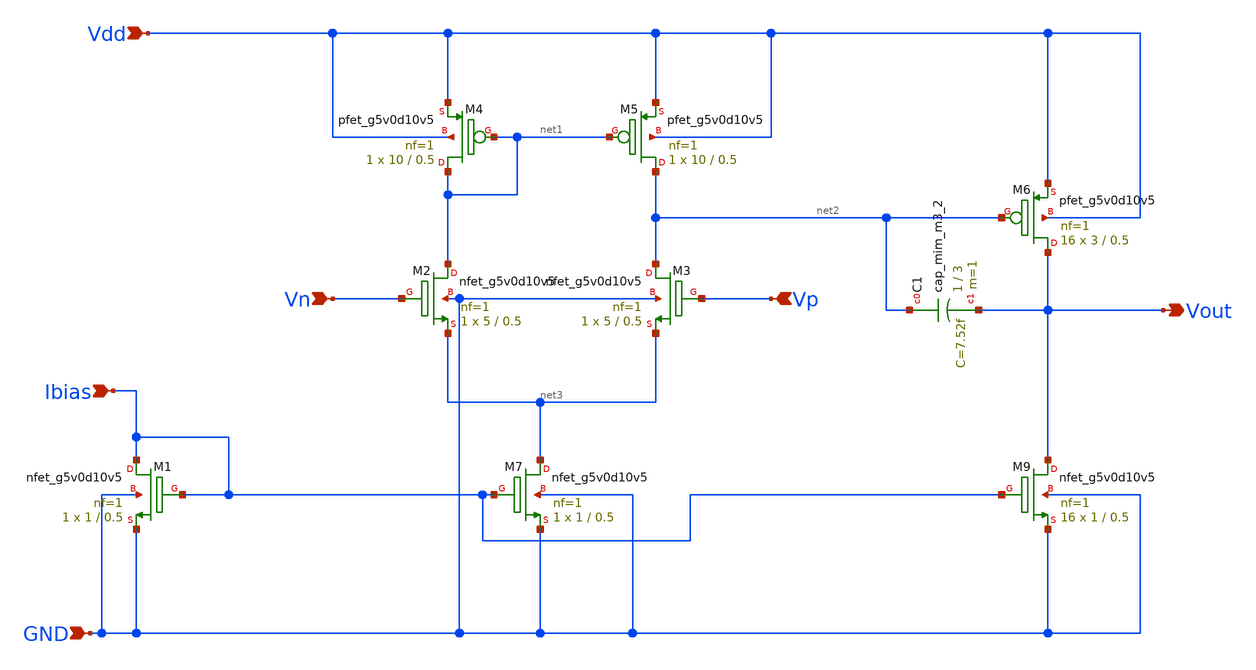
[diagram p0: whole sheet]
** sch_path: Analog_Blocks/LDO/Schematic/LDO_Miller_1.8v/Error_Amplifier.sch
**.subckt Error_Amplifier Vout Vdd GND Vp Vn Ibias
*.opin Vout
*.ipin Vdd
*.ipin GND
*.ipin Vp
*.ipin Vn
*.ipin Ibias
XM2 net1 Vn net3 GND sky130_fd_pr__nfet_g5v0d10v5 L=0.5 W=5 nf=1 ad='int((nf+1)/2) * W/nf * 0.29' as='int((nf+2)/2) * W/nf * 0.29'
+ pd='2*int((nf+1)/2) * (W/nf + 0.29)' ps='2*int((nf+2)/2) * (W/nf + 0.29)' nrd='0.29 / W' nrs='0.29 / W'
+ sa=0 sb=0 sd=0 mult=1 m=1
XM3 net2 Vp net3 GND sky130_fd_pr__nfet_g5v0d10v5 L=0.5 W=5 nf=1 ad='int((nf+1)/2) * W/nf * 0.29' as='int((nf+2)/2) * W/nf * 0.29'
+ pd='2*int((nf+1)/2) * (W/nf + 0.29)' ps='2*int((nf+2)/2) * (W/nf + 0.29)' nrd='0.29 / W' nrs='0.29 / W'
+ sa=0 sb=0 sd=0 mult=1 m=1
XM4 net1 net1 Vdd Vdd sky130_fd_pr__pfet_g5v0d10v5 L=0.5 W=10 nf=1 ad='int((nf+1)/2) * W/nf * 0.29' as='int((nf+2)/2) * W/nf * 0.29'
+ pd='2*int((nf+1)/2) * (W/nf + 0.29)' ps='2*int((nf+2)/2) * (W/nf + 0.29)' nrd='0.29 / W' nrs='0.29 / W'
+ sa=0 sb=0 sd=0 mult=1 m=1
XM5 net2 net1 Vdd Vdd sky130_fd_pr__pfet_g5v0d10v5 L=0.5 W=10 nf=1 ad='int((nf+1)/2) * W/nf * 0.29' as='int((nf+2)/2) * W/nf * 0.29'
+ pd='2*int((nf+1)/2) * (W/nf + 0.29)' ps='2*int((nf+2)/2) * (W/nf + 0.29)' nrd='0.29 / W' nrs='0.29 / W'
+ sa=0 sb=0 sd=0 mult=1 m=1
XM6 Vout net2 Vdd Vdd sky130_fd_pr__pfet_g5v0d10v5 L=0.5 W=3 nf=1 ad='int((nf+1)/2) * W/nf * 0.29' as='int((nf+2)/2) * W/nf * 0.29'
+ pd='2*int((nf+1)/2) * (W/nf + 0.29)' ps='2*int((nf+2)/2) * (W/nf + 0.29)' nrd='0.29 / W' nrs='0.29 / W'
+ sa=0 sb=0 sd=0 mult=16 m=16
XM7 net3 Ibias GND GND sky130_fd_pr__nfet_g5v0d10v5 L=0.5 W=1 nf=1 ad='int((nf+1)/2) * W/nf * 0.29' as='int((nf+2)/2) * W/nf * 0.29'
+ pd='2*int((nf+1)/2) * (W/nf + 0.29)' ps='2*int((nf+2)/2) * (W/nf + 0.29)' nrd='0.29 / W' nrs='0.29 / W'
+ sa=0 sb=0 sd=0 mult=1 m=1
XM9 Vout Ibias GND GND sky130_fd_pr__nfet_g5v0d10v5 L=0.5 W=1 nf=1 ad='int((nf+1)/2) * W/nf * 0.29' as='int((nf+2)/2) * W/nf * 0.29'
+ pd='2*int((nf+1)/2) * (W/nf + 0.29)' ps='2*int((nf+2)/2) * (W/nf + 0.29)' nrd='0.29 / W' nrs='0.29 / W'
+ sa=0 sb=0 sd=0 mult=16 m=16
XM1 Ibias Ibias GND GND sky130_fd_pr__nfet_g5v0d10v5 L=0.5 W=1 nf=1 ad='int((nf+1)/2) * W/nf * 0.29'
+ as='int((nf+2)/2) * W/nf * 0.29' pd='2*int((nf+1)/2) * (W/nf + 0.29)' ps='2*int((nf+2)/2) * (W/nf + 0.29)'
+ nrd='0.29 / W' nrs='0.29 / W' sa=0 sb=0 sd=0 mult=1 m=1
XC1 net2 Vout sky130_fd_pr__cap_mim_m3_2 W=1 L=3 MF=1 m=1
**.ends
.end
